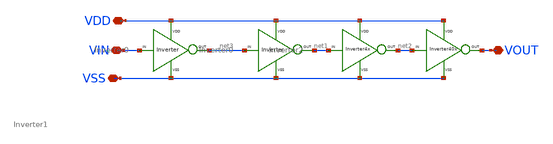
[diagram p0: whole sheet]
** sch_path: xschem/DC_DC_Converter_xschem/OTHERS/DC_DC_Converter_2/DC_DC_Converter/BUFFER/BUFFER_PMOS/BUFFER_P.sch
**.subckt BUFFER_P VDD VIN VSS VOUT
*.iopin VDD
*.iopin VIN
*.iopin VSS
*.iopin VOUT
X7 net3 net1 VDD VSS Inverter0
X8 net1 net2 VDD VSS Inverter1
X1 net2 VOUT VDD VSS Inverter2
X2 VIN net3 VDD VSS Inverter0
**.ends
.end
